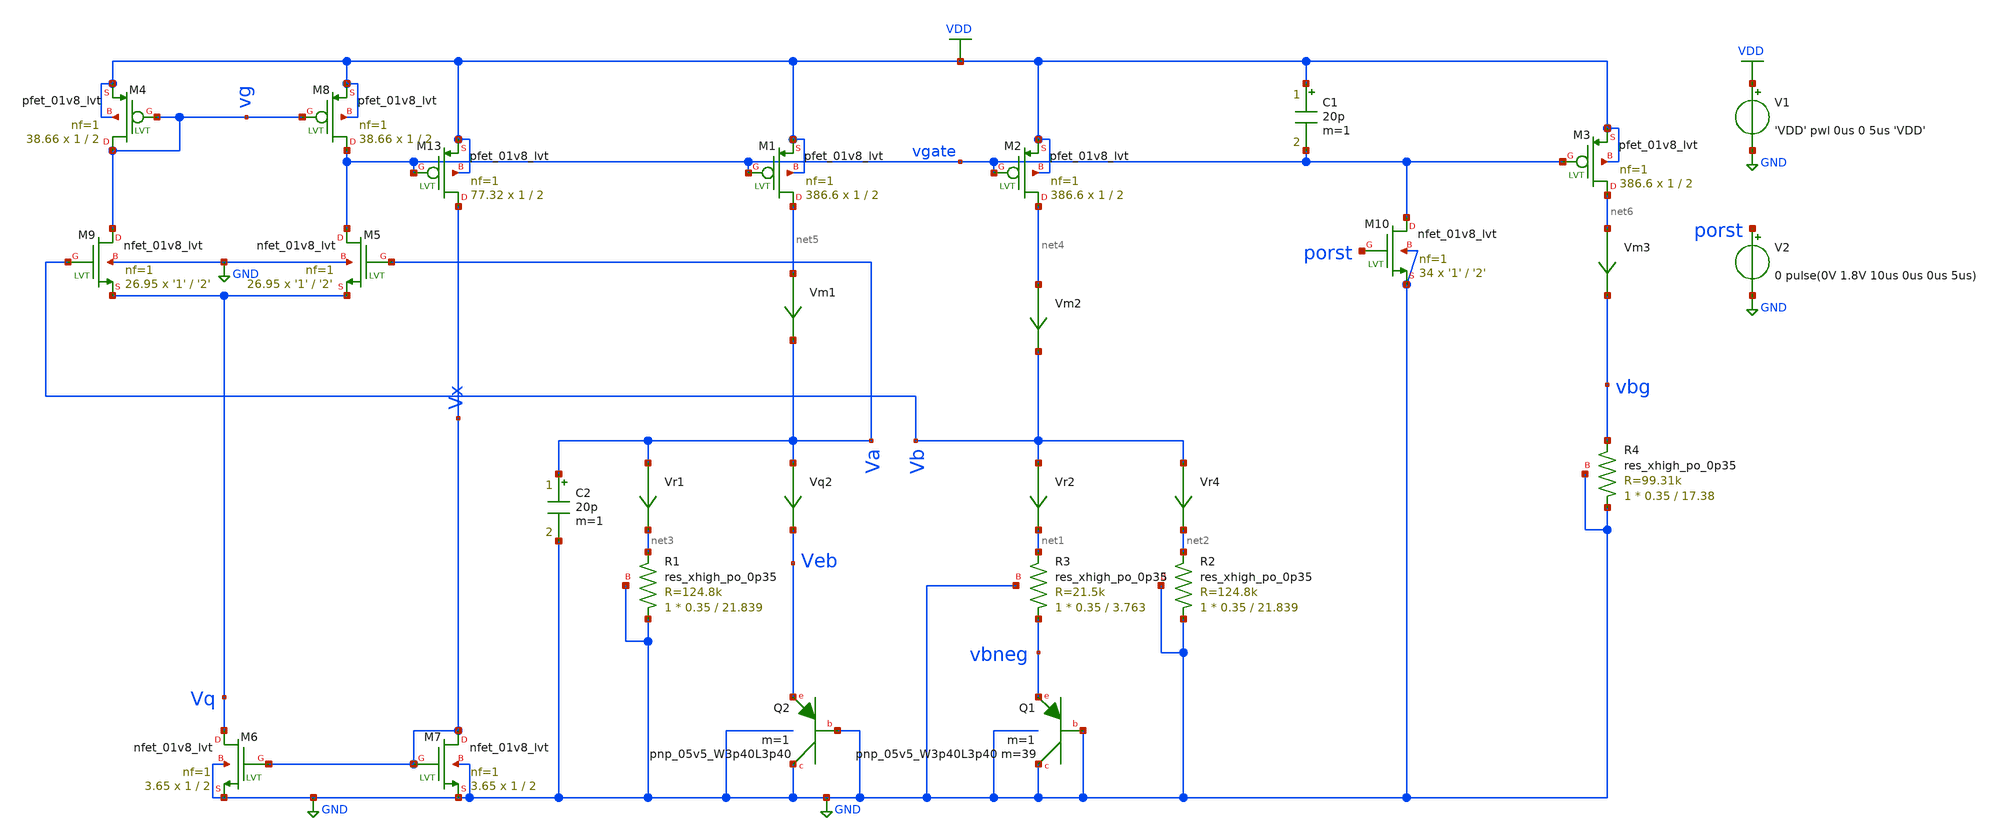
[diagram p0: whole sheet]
** sch_path: VLSI23/bandgap_sky130_v1/tests/tran_gauss/tsmc_bandgap_real_tran_gauss.sch
**.subckt tsmc_bandgap_real_tran_gauss
V1 VDD GND 'VDD' pwl 0us 0 5us 'VDD'
XQ2 GND GND Veb sky130_fd_pr__pnp_05v5_W3p40L3p40 m=1
Vr4 Vb net2 0
.save i(vr4)
Vr2 Vb net1 0
.save i(vr2)
Vm1 net5 Va 0
.save i(vm1)
Vm2 net4 Vb 0
.save i(vm2)
Vm3 net6 vbg 0
.save i(vm3)
Vr1 Va net3 0
.save i(vr1)
Vq2 Va Veb 0
.save i(vq2)
XQ1 GND GND vbneg sky130_fd_pr__pnp_05v5_W3p40L3p40 m=39 m=1
XM5 vgate Va Vq GND sky130_fd_pr__nfet_01v8_lvt L='2' W='1' nf=1 ad='int((nf+1)/2) * W/nf * 0.29' as='int((nf+2)/2) * W/nf * 0.29'
+ pd='2*int((nf+1)/2) * (W/nf + 0.29)' ps='2*int((nf+2)/2) * (W/nf + 0.29)' nrd='0.29 / W' nrs='0.29 / W'
+ sa=0 sb=0 sd=0 mult=26.95 m=26.95
XM6 Vq Vx GND GND sky130_fd_pr__nfet_01v8_lvt L=2 W=1 nf=1 ad='int((nf+1)/2) * W/nf * 0.29' as='int((nf+2)/2) * W/nf * 0.29'
+ pd='2*int((nf+1)/2) * (W/nf + 0.29)' ps='2*int((nf+2)/2) * (W/nf + 0.29)' nrd='0.29 / W' nrs='0.29 / W'
+ sa=0 sb=0 sd=0 mult=3.65 m=3.65
XM9 vg Vb Vq GND sky130_fd_pr__nfet_01v8_lvt L='2' W='1' nf=1 ad='int((nf+1)/2) * W/nf * 0.29' as='int((nf+2)/2) * W/nf * 0.29'
+ pd='2*int((nf+1)/2) * (W/nf + 0.29)' ps='2*int((nf+2)/2) * (W/nf + 0.29)' nrd='0.29 / W' nrs='0.29 / W'
+ sa=0 sb=0 sd=0 mult=26.95 m=26.95
XM7 Vx Vx GND GND sky130_fd_pr__nfet_01v8_lvt L=2 W=1 nf=1 ad='int((nf+1)/2) * W/nf * 0.29' as='int((nf+2)/2) * W/nf * 0.29'
+ pd='2*int((nf+1)/2) * (W/nf + 0.29)' ps='2*int((nf+2)/2) * (W/nf + 0.29)' nrd='0.29 / W' nrs='0.29 / W'
+ sa=0 sb=0 sd=0 mult=3.65 m=3.65
XM13 Vx vgate VDD VDD sky130_fd_pr__pfet_01v8_lvt L=2 W=1 nf=1 ad='int((nf+1)/2) * W/nf * 0.29' as='int((nf+2)/2) * W/nf * 0.29'
+ pd='2*int((nf+1)/2) * (W/nf + 0.29)' ps='2*int((nf+2)/2) * (W/nf + 0.29)' nrd='0.29 / W' nrs='0.29 / W'
+ sa=0 sb=0 sd=0 mult=77.32 m=77.32
XM1 net5 vgate VDD VDD sky130_fd_pr__pfet_01v8_lvt L=2 W=1 nf=1 ad='int((nf+1)/2) * W/nf * 0.29' as='int((nf+2)/2) * W/nf * 0.29'
+ pd='2*int((nf+1)/2) * (W/nf + 0.29)' ps='2*int((nf+2)/2) * (W/nf + 0.29)' nrd='0.29 / W' nrs='0.29 / W'
+ sa=0 sb=0 sd=0 mult=386.6 m=386.6
XM2 net4 vgate VDD VDD sky130_fd_pr__pfet_01v8_lvt L=2 W=1 nf=1 ad='int((nf+1)/2) * W/nf * 0.29' as='int((nf+2)/2) * W/nf * 0.29'
+ pd='2*int((nf+1)/2) * (W/nf + 0.29)' ps='2*int((nf+2)/2) * (W/nf + 0.29)' nrd='0.29 / W' nrs='0.29 / W'
+ sa=0 sb=0 sd=0 mult=386.6 m=386.6
XM3 net6 vgate VDD VDD sky130_fd_pr__pfet_01v8_lvt L=2 W=1 nf=1 ad='int((nf+1)/2) * W/nf * 0.29' as='int((nf+2)/2) * W/nf * 0.29'
+ pd='2*int((nf+1)/2) * (W/nf + 0.29)' ps='2*int((nf+2)/2) * (W/nf + 0.29)' nrd='0.29 / W' nrs='0.29 / W'
+ sa=0 sb=0 sd=0 mult=386.6 m=386.6
XR1 GND net3 GND sky130_fd_pr__res_xhigh_po_0p35 L=21.839 mult=1 m=1
XR2 GND net2 GND sky130_fd_pr__res_xhigh_po_0p35 L=21.839 mult=1 m=1
XR3 vbneg net1 GND sky130_fd_pr__res_xhigh_po_0p35 L=3.763 mult=1 m=1
XR4 GND vbg GND sky130_fd_pr__res_xhigh_po_0p35 L=17.38 mult=1 m=1
XM4 vg vg VDD VDD sky130_fd_pr__pfet_01v8_lvt L=2 W=1 nf=1 ad='int((nf+1)/2) * W/nf * 0.29' as='int((nf+2)/2) * W/nf * 0.29'
+ pd='2*int((nf+1)/2) * (W/nf + 0.29)' ps='2*int((nf+2)/2) * (W/nf + 0.29)' nrd='0.29 / W' nrs='0.29 / W'
+ sa=0 sb=0 sd=0 mult=38.66 m=38.66
XM8 vgate vg VDD VDD sky130_fd_pr__pfet_01v8_lvt L=2 W=1 nf=1 ad='int((nf+1)/2) * W/nf * 0.29' as='int((nf+2)/2) * W/nf * 0.29'
+ pd='2*int((nf+1)/2) * (W/nf + 0.29)' ps='2*int((nf+2)/2) * (W/nf + 0.29)' nrd='0.29 / W' nrs='0.29 / W'
+ sa=0 sb=0 sd=0 mult=38.66 m=38.66
XM10 vgate porst GND GND sky130_fd_pr__nfet_01v8_lvt L='2' W='1' nf=1 ad='int((nf+1)/2) * W/nf * 0.29'
+ as='int((nf+2)/2) * W/nf * 0.29' pd='2*int((nf+1)/2) * (W/nf + 0.29)' ps='2*int((nf+2)/2) * (W/nf + 0.29)'
+ nrd='0.29 / W' nrs='0.29 / W' sa=0 sb=0 sd=0 mult=34 m=34
V2 porst GND 0 pulse(0V 1.8V 10us 0us 0us 5us)
C1 VDD vgate 20p m=1
C2 Va GND 20p m=1
**** begin user architecture code

.include $::SKYWATER_MODELS/cells/nfet_01v8/sky130_fd_pr__nfet_01v8__tt.corner.spice
.include $::SKYWATER_MODELS/cells/nfet_01v8_lvt/sky130_fd_pr__nfet_01v8_lvt__tt.corner.spice
.include $::SKYWATER_MODELS/cells/pfet_01v8/sky130_fd_pr__pfet_01v8__tt.corner.spice
.include $::SKYWATER_MODELS/cells/nfet_03v3_nvt/sky130_fd_pr__nfet_03v3_nvt__tt.corner.spice
.include $::SKYWATER_MODELS/cells/nfet_05v0_nvt/sky130_fd_pr__nfet_05v0_nvt__tt.corner.spice
.include $::SKYWATER_MODELS/cells/esd_nfet_01v8/sky130_fd_pr__esd_nfet_01v8__tt.corner.spice
.include $::SKYWATER_MODELS/cells/pfet_01v8_lvt/sky130_fd_pr__pfet_01v8_lvt__tt.corner.spice
.include $::SKYWATER_MODELS/cells/pfet_01v8_hvt/sky130_fd_pr__pfet_01v8_hvt__tt.corner.spice
.include $::SKYWATER_MODELS/cells/esd_pfet_g5v0d10v5/sky130_fd_pr__esd_pfet_g5v0d10v5__tt.corner.spice
.include $::SKYWATER_MODELS/cells/pfet_g5v0d10v5/sky130_fd_pr__pfet_g5v0d10v5__tt.corner.spice
.include $::SKYWATER_MODELS/cells/pfet_g5v0d16v0/sky130_fd_pr__pfet_g5v0d16v0__tt.corner.spice
.include $::SKYWATER_MODELS/cells/nfet_g5v0d10v5/sky130_fd_pr__nfet_g5v0d10v5__tt.corner.spice
.include $::SKYWATER_MODELS/cells/nfet_g5v0d16v0/sky130_fd_pr__nfet_g5v0d16v0__tt_discrete.corner.spice
.include $::SKYWATER_MODELS/cells/esd_nfet_g5v0d10v5/sky130_fd_pr__esd_nfet_g5v0d10v5__tt.corner.spice
.include $::SKYWATER_MODELS/models/corners/tt/nonfet.spice
* Mismatch parameters
.include $::SKYWATER_MODELS/cells/nfet_01v8/sky130_fd_pr__nfet_01v8__mismatch.corner.spice
.include $::SKYWATER_MODELS/cells/pfet_01v8/sky130_fd_pr__pfet_01v8__mismatch.corner.spice
.include $::SKYWATER_MODELS/cells/nfet_01v8_lvt/sky130_fd_pr__nfet_01v8_lvt__mismatch.corner.spice
.include $::SKYWATER_MODELS/cells/pfet_01v8_lvt/sky130_fd_pr__pfet_01v8_lvt__mismatch.corner.spice
.include $::SKYWATER_MODELS/cells/pfet_01v8_hvt/sky130_fd_pr__pfet_01v8_hvt__mismatch.corner.spice
.include $::SKYWATER_MODELS/cells/nfet_g5v0d10v5/sky130_fd_pr__nfet_g5v0d10v5__mismatch.corner.spice
.include $::SKYWATER_MODELS/cells/pfet_g5v0d10v5/sky130_fd_pr__pfet_g5v0d10v5__mismatch.corner.spice
.include $::SKYWATER_MODELS/cells/nfet_05v0_nvt/sky130_fd_pr__nfet_05v0_nvt__mismatch.corner.spice
.include $::SKYWATER_MODELS/cells/nfet_03v3_nvt/sky130_fd_pr__nfet_03v3_nvt__mismatch.corner.spice
* Resistor$::SKYWATER_MODELS/Capacitor
.include $::SKYWATER_MODELS/models/r+c/res_typical__cap_typical.spice
.include $::SKYWATER_MODELS/models/r+c/res_typical__cap_typical__lin.spice
* Special cells
.include $::SKYWATER_MODELS/models/corners/tt/specialized_cells.spice
* All models
.include $::SKYWATER_MODELS/models/all.spice
.include $::SKYWATER_MODELS/cells/pnp_05v5/sky130_fd_pr__pnp_05v5_W3p40L3p40.model.spice
* Corner
.include $::SKYWATER_MODELS/models/corners/tt/rf.spice


.option seed=13

.param ABSVAR=0.03
.param VDDGAUSS=agauss(1.8, 'ABSVAR', 1)
.param VDD=VDDGAUSS
*.param VDD=1.8
** variation parameters:
.param sky130_fd_pr__nfet_01v8_lvt__vth0_slope_spectre='agauss(0, ABSVAR, 3)/sky130_fd_pr__nfet_01v8_lvt__vth0_slope'
.param sky130_fd_pr__pfet_01v8_lvt__vth0_slope_spectre='agauss(0, ABSVAR, 3)/sky130_fd_pr__pfet_01v8_lvt__vth0_slope'
.param sky130_fd_pr__pfet_01v8_lvt__toxe_slope_spectre='agauss(0, ABSVAR*2, 3)/sky130_fd_pr__pfet_01v8_lvt__toxe_slope'
.param sky130_fd_pr__nfet_01v8_lvt__toxe_slope_spectre='agauss(0, ABSVAR*2, 3)/sky130_fd_pr__nfet_01v8_lvt__toxe_slope'
.param sky130_fd_pr__pfet_01v8_lvt__voff_slope_spectre='agauss(0, ABSVAR, 3)/sky130_fd_pr__pfet_01v8_lvt__voff_slope'
.param sky130_fd_pr__nfet_01v8_lvt__voff_slope_spectre='agauss(0, ABSVAR, 3)/sky130_fd_pr__nfet_01v8_lvt__voff_slope'
.param sky130_fd_pr__pfet_01v8_lvt__nfactor_slope_spectre='agauss(0, ABSVAR, 3)/sky130_fd_pr__pfet_01v8_lvt__nfactor_slope'
.param sky130_fd_pr__nfet_01v8_lvt__nfactor_slope_spectre='agauss(0, ABSVAR, 3)/sky130_fd_pr__nfet_01v8_lvt__nfactor_slope'

.param sky130_fd_pr__res_xhigh_po__var_mult=agauss(0, 'ABSVAR*8', 1)
.param sky130_fd_pr__res_high_po_var=agauss(0, 'ABSVAR*8', 1)

.param sky130_fd_pr__pnp_05v5_W3p40L3p40__bf_slope=agauss(0, 0.05537, 1)
.param sky130_fd_pr__pnp_05v5_W3p40L3p40__is_slope=agauss(0, 0.01662, 1)
.param sky130_fd_pr__pnp_05v5_W3p40L3p40__xti_slope=agauss(0, 0.06, 1)
* .options savecurrents
.control
  let run=1
  dowhile run <= 40
    if run > 1
      reset
      set appendwrite
    end
    save all
    if run % 3 = 0
      set temp=0
    end
    if run % 3 = 1
      set temp=27
    end
    if run % 3 = 2
      set temp=70
    end
    tran 0.05u 150u
    write ./sims/tsmc_bandgap_real_tran_gauss{$&run}.raw vbg vdd
    let run = run + 1
  end
  set nolegend
  *plot all.vbg
  unset askquit
  quit
.endc


**** end user architecture code
**.ends
.GLOBAL VDD
.GLOBAL GND
.end
